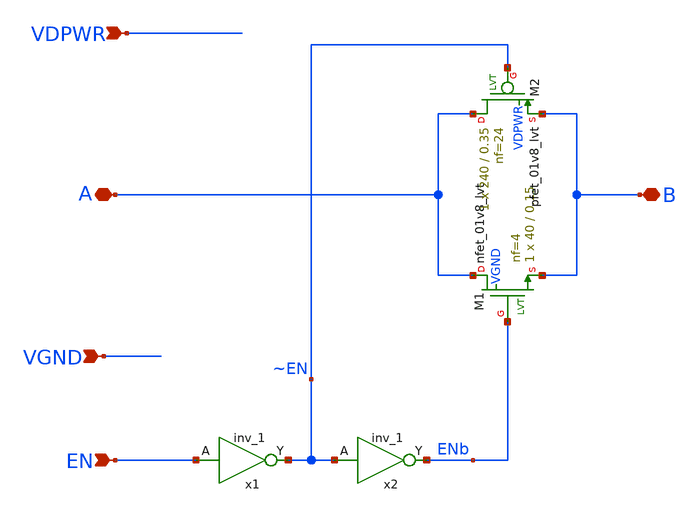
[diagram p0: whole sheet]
** sch_path: xschem/switch.sch
**.subckt switch EN VDPWR VGND B A
*.ipin EN
*.ipin VDPWR
*.ipin VGND
*.iopin B
*.iopin A
XM1 A ENb B VGND sky130_fd_pr__nfet_01v8_lvt L=0.15 W=40 nf=4 ad='int((4 + 1)/2) * 40 / 4 * 0.29' as='int((4 + 2)/2) * 40 / 4 * 0.29'
+ pd='2*int((4 + 1)/2) * (40 / 4 + 0.29)' ps='2*int((4 + 2)/2) * (40 / 4 + 0.29)' nrd='0.29 / 40 ' nrs='0.29 / 40 '
+ sa=0 sb=0 sd=0 mult=1 m=1
XM2 A ~EN B VDPWR sky130_fd_pr__pfet_01v8_lvt L=0.35 W=240 nf=24 ad='int((24 + 1)/2) * 240 / 24 * 0.29'
+ as='int((24 + 2)/2) * 240 / 24 * 0.29' pd='2*int((24 + 1)/2) * (240 / 24 + 0.29)' ps='2*int((24 + 2)/2) * (240 / 24 + 0.29)'
+ nrd='0.29 / 240 ' nrs='0.29 / 240 ' sa=0 sb=0 sd=0 mult=1 m=1
x1 EN VGND VGND VDPWR VDPWR ~EN sky130_fd_sc_hd__inv_1
x2 ~EN VGND VGND VDPWR VDPWR ENb sky130_fd_sc_hd__inv_1
**.ends
.end
